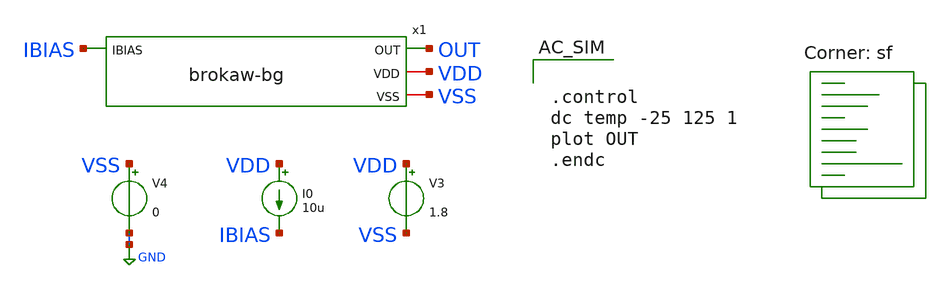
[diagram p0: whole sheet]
** sch_path: designs/libs/core_analog/core_bandgap/brokaw-bandgap/tb_brokaw-bg.sch
**.subckt tb_brokaw-bg
V3 VDD VSS 1.8
V4 VSS GND 0
I0 VDD IBIAS 10u
x1 IBIAS OUT VDD VSS brokaw-bg
**** begin user architecture code
.lib $::SKYWATER_MODELS/sky130.lib.spice sf


.control
dc temp -25 125 1
plot OUT
.endc


**** end user architecture code
**.ends

* expanding   symbol:
*+  bandgap-referenced-ota/designs/libs/core_analog/core_bandgap/brokaw-bandgap/brokaw-bg.sym # of pins=4
** sym_path: designs/libs/core_analog/core_bandgap/brokaw-bandgap/brokaw-bg.sym
** sch_path: designs/libs/core_analog/core_bandgap/brokaw-bandgap/brokaw-bg.sch
.subckt brokaw-bg IBIAS OUT VDD VSS
*.iopin VDD
*.iopin VSS
*.opin OUT
*.ipin IBIAS
XR1 net1 VDD VSS sky130_fd_pr__res_xhigh_po W=1 L=1.25 mult=1 m=1
XR2 net2 VDD VSS sky130_fd_pr__res_xhigh_po W=1 L=1.25 mult=1 m=1
XQ1 net1 OUT net3 VSS sky130_fd_pr__npn_05v5_w1p00l2p00
XQ2 net2 OUT net4 VSS sky130_fd_pr__npn_05v5_w1p00l2p00
x1 net1 OUT IBIAS VSS net2 VDD n-ota-bg
XR3 net4 net3 VSS sky130_fd_pr__res_xhigh_po W=1 L=2 mult=1 m=1
XR4 VSS net4 VSS sky130_fd_pr__res_xhigh_po W=19 L=1 mult=1 m=1
.ends


* expanding   symbol:
*+  bandgap-referenced-ota/designs/libs/core_analog/core_bandgap/5t-ota/n-ota-bg.sym # of pins=6
** sym_path: designs/libs/core_analog/core_bandgap/5t-ota/n-ota-bg.sym
** sch_path: designs/libs/core_analog/core_bandgap/5t-ota/n-ota-bg.sch
.subckt n-ota-bg VN OUT IBIAS VSS VP VDD
*.iopin VDD
*.iopin VSS
*.ipin IBIAS
*.ipin VP
*.ipin VN
*.opin OUT
XM1 net2 VP net1 VSS sky130_fd_pr__nfet_01v8 L=4 W=4 nf=1 ad='int((nf+1)/2) * W/nf * 0.29' as='int((nf+2)/2) * W/nf * 0.29'
+ pd='2*int((nf+1)/2) * (W/nf + 0.29)' ps='2*int((nf+2)/2) * (W/nf + 0.29)' nrd='0.29 / W' nrs='0.29 / W'
+ sa=0 sb=0 sd=0 mult=1 m=1
XM2 net3 VN net1 VSS sky130_fd_pr__nfet_01v8 L=4 W=4 nf=1 ad='int((nf+1)/2) * W/nf * 0.29' as='int((nf+2)/2) * W/nf * 0.29'
+ pd='2*int((nf+1)/2) * (W/nf + 0.29)' ps='2*int((nf+2)/2) * (W/nf + 0.29)' nrd='0.29 / W' nrs='0.29 / W'
+ sa=0 sb=0 sd=0 mult=1 m=1
XM3 net1 IBIAS VSS VSS sky130_fd_pr__nfet_01v8 L=4 W=4 nf=1 ad='int((nf+1)/2) * W/nf * 0.29' as='int((nf+2)/2) * W/nf * 0.29'
+ pd='2*int((nf+1)/2) * (W/nf + 0.29)' ps='2*int((nf+2)/2) * (W/nf + 0.29)' nrd='0.29 / W' nrs='0.29 / W'
+ sa=0 sb=0 sd=0 mult=1 m=1
XM4 net3 net2 VDD VDD sky130_fd_pr__pfet_01v8 L=4 W=8 nf=1 ad='int((nf+1)/2) * W/nf * 0.29' as='int((nf+2)/2) * W/nf * 0.29'
+ pd='2*int((nf+1)/2) * (W/nf + 0.29)' ps='2*int((nf+2)/2) * (W/nf + 0.29)' nrd='0.29 / W' nrs='0.29 / W'
+ sa=0 sb=0 sd=0 mult=1 m=1
XM5 net2 net2 VDD VDD sky130_fd_pr__pfet_01v8 L=4 W=8 nf=1 ad='int((nf+1)/2) * W/nf * 0.29' as='int((nf+2)/2) * W/nf * 0.29'
+ pd='2*int((nf+1)/2) * (W/nf + 0.29)' ps='2*int((nf+2)/2) * (W/nf + 0.29)' nrd='0.29 / W' nrs='0.29 / W'
+ sa=0 sb=0 sd=0 mult=1 m=1
XM6 IBIAS IBIAS VSS VSS sky130_fd_pr__nfet_01v8 L=4 W=4 nf=1 ad='int((nf+1)/2) * W/nf * 0.29' as='int((nf+2)/2) * W/nf * 0.29'
+ pd='2*int((nf+1)/2) * (W/nf + 0.29)' ps='2*int((nf+2)/2) * (W/nf + 0.29)' nrd='0.29 / W' nrs='0.29 / W'
+ sa=0 sb=0 sd=0 mult=1 m=1
XM7 net3 net2 VDD VDD sky130_fd_pr__pfet_01v8 L=4 W=8 nf=1 ad='int((nf+1)/2) * W/nf * 0.29' as='int((nf+2)/2) * W/nf * 0.29'
+ pd='2*int((nf+1)/2) * (W/nf + 0.29)' ps='2*int((nf+2)/2) * (W/nf + 0.29)' nrd='0.29 / W' nrs='0.29 / W'
+ sa=0 sb=0 sd=0 mult=1 m=1
XM8 net2 net2 VDD VDD sky130_fd_pr__pfet_01v8 L=4 W=8 nf=1 ad='int((nf+1)/2) * W/nf * 0.29' as='int((nf+2)/2) * W/nf * 0.29'
+ pd='2*int((nf+1)/2) * (W/nf + 0.29)' ps='2*int((nf+2)/2) * (W/nf + 0.29)' nrd='0.29 / W' nrs='0.29 / W'
+ sa=0 sb=0 sd=0 mult=1 m=1
XM9 OUT net3 VDD VDD sky130_fd_pr__pfet_01v8 L=2 W=18 nf=1 ad='int((nf+1)/2) * W/nf * 0.29' as='int((nf+2)/2) * W/nf * 0.29'
+ pd='2*int((nf+1)/2) * (W/nf + 0.29)' ps='2*int((nf+2)/2) * (W/nf + 0.29)' nrd='0.29 / W' nrs='0.29 / W'
+ sa=0 sb=0 sd=0 mult=1 m=1
XM10 OUT IBIAS VSS VSS sky130_fd_pr__nfet_01v8 L=2 W=2 nf=1 ad='int((nf+1)/2) * W/nf * 0.29' as='int((nf+2)/2) * W/nf * 0.29'
+ pd='2*int((nf+1)/2) * (W/nf + 0.29)' ps='2*int((nf+2)/2) * (W/nf + 0.29)' nrd='0.29 / W' nrs='0.29 / W'
+ sa=0 sb=0 sd=0 mult=1 m=1
XC1 OUT net3 sky130_fd_pr__cap_mim_m3_1 W=25 L=1 MF=1 m=1
.ends

.GLOBAL GND
.end
